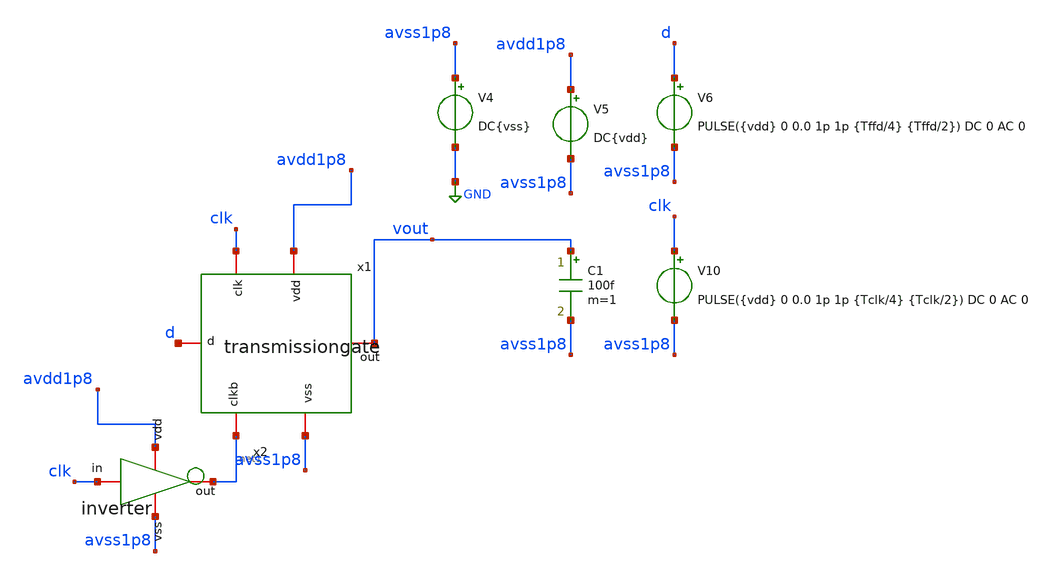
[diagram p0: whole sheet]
** sch_path: verification/testbenches/transmissiongate/tb_transmisiongate.sch
**.subckt tb_transmisiongate
C1 vout avss1p8 100f m=1
V4 avss1p8 GND DC{vss}
V6 d avss1p8 PULSE({vdd} 0 0.0 1p 1p {Tffd/4} {Tffd/2}) DC 0 AC 0
x1 clk avss1p8 vout d avdd1p8 net1 transmissiongate
V10 clk avss1p8 PULSE({vdd} 0 0.0 1p 1p {Tclk/4} {Tclk/2}) DC 0 AC 0
x2 avdd1p8 net1 clk avss1p8 inverter
V5 avdd1p8 avss1p8 DC{vdd}
**** begin user architecture code


* Circuit Parameters
.param vdd = 1.2
.param vss = 0.0
.param Tclk = 10n
.param Tffd = 85n
.options TEMP = 27.0
* Include Models - IHP SG13G2
.lib cornerMOSlv.lib mos_tt
* OP Parameters & Singals to save
.save all
*Simulations
.control
tran 0.01u 100n
setplot tran1
plot v(d) v(clk)+1.2 v(vout)+2.4
reset
dc V6 0 1.2 0.01
setplot dc
plot vin vout ylabel vout xlabel vin
set filetype = ascii
write dcsweep.raw
.endc
.end


**** end user architecture code
**.ends

* expanding   symbol:  blocks/transmissiongate/schematic/transmissiongate.sym # of pins=6
** sym_path: design/blocks/transmissiongate/schematic/transmissiongate.sym
** sch_path: design/blocks/transmissiongate/schematic/transmissiongate.sch
.subckt transmissiongate clk vss out d vdd clkb
*.iopin out
*.iopin d
*.iopin clkb
*.iopin clk
*.iopin vdd
*.iopin vss
XM1 out clkb d vdd sg13_lv_pmos w=1.5u l=0.15u ng=1 m=1 mm_ok=1
XM0 d clk out vss sg13_lv_nmos w=0.75u l=0.15u ng=1 m=1 mm_ok=1
.ends


* expanding   symbol:  blocks/inverter/schematic/inverter.sym # of pins=4
** sym_path: design/blocks/inverter/schematic/inverter.sym
** sch_path: design/blocks/inverter/schematic/inverter.sch
.subckt inverter vdd out in vss
*.iopin vdd
*.iopin out
*.iopin vss
*.iopin in
XM1 out in vss vss sg13_lv_nmos w=0.75u l=0.15u ng=1 m=1 mm_ok=1
XM2 out in vdd vdd sg13_lv_pmos w=1.5u l=0.15u ng=1 m=1 mm_ok=1
.ends

.GLOBAL GND
.end
